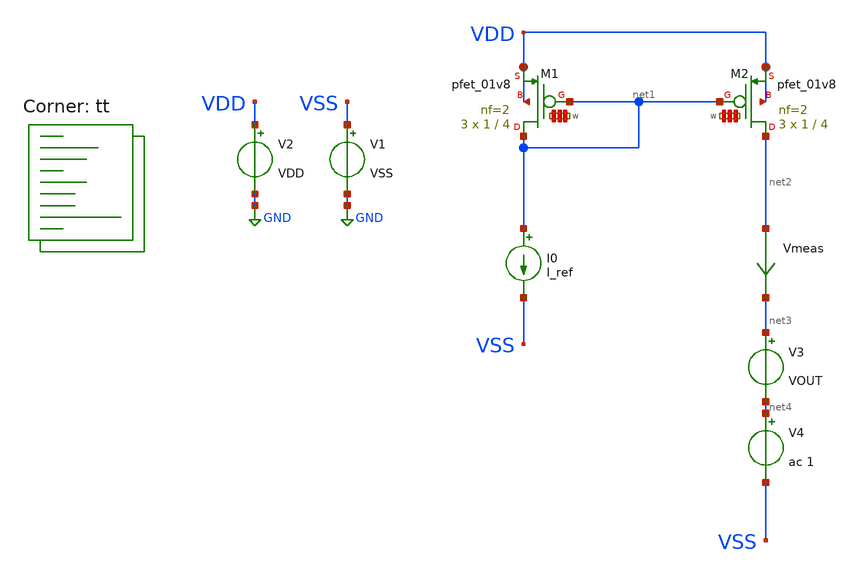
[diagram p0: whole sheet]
** sch_path: Learning/Current_mirrors/Design_pmos_current_mirror_sky130_5v/simulation/test.sch
**.subckt test
V1 VSS GND VSS
V2 VDD GND VDD
I0 net1 VSS I_ref
Vmeas net2 net3 0
.save i(vmeas)
V3 net3 net4 VOUT
XM1 net1 net1 VDD VDD sky130_fd_pr__pfet_01v8 L=4 W='1 * 2 ' nf=2 ad= as='int((2 + 2)/2) * 1 * 0.29'
+ pd='2*int((2 + 1)/2) * (1 + 0.29)' ps='2*int((2 + 2)/2) * (1 + 0.29)' nrd='0.29 / 1 / 2 ' nrs='0.29 / 1 / 2 '
+ sa=0 sb=0 sd=0 mult=3 m=3
V4 net4 VSS ac 1
XM2 net2 net1 VDD VDD sky130_fd_pr__pfet_01v8 L=4 W='1 * 2 ' nf=2 ad= as='int((2 + 2)/2) * 1 * 0.29'
+ pd='2*int((2 + 1)/2) * (1 + 0.29)' ps='2*int((2 + 2)/2) * (1 + 0.29)' nrd='0.29 / 1 / 2 ' nrs='0.29 / 1 / 2 '
+ sa=0 sb=0 sd=0 mult=3 m=3
**** begin user architecture code
.lib $::SKYWATER_MODELS/sky130.lib.spice tt
**** end user architecture code
**.ends
.GLOBAL GND
**** begin user architecture code



.param VDD = 1.8
.param VSS = 0
.param I_ref = 5u
.param VOUT = 0.9

.control
op
print @m.xm1.msky130_fd_pr__pfet_01v8[vdsat]
print @m.xm1.msky130_fd_pr__pfet_01v8[vth]
print 1/@m.xm1.msky130_fd_pr__pfet_01v8[gds]
print @m.xm1.msky130_fd_pr__pfet_01v8[gm]

dc V3 0 1.8 0.01
plot i(Vmeas)
plot 1/deriv(i(Vmeas))
ac dec 100 1 10G
plot i(Vmeas)

.endc



**** end user architecture code
.end
